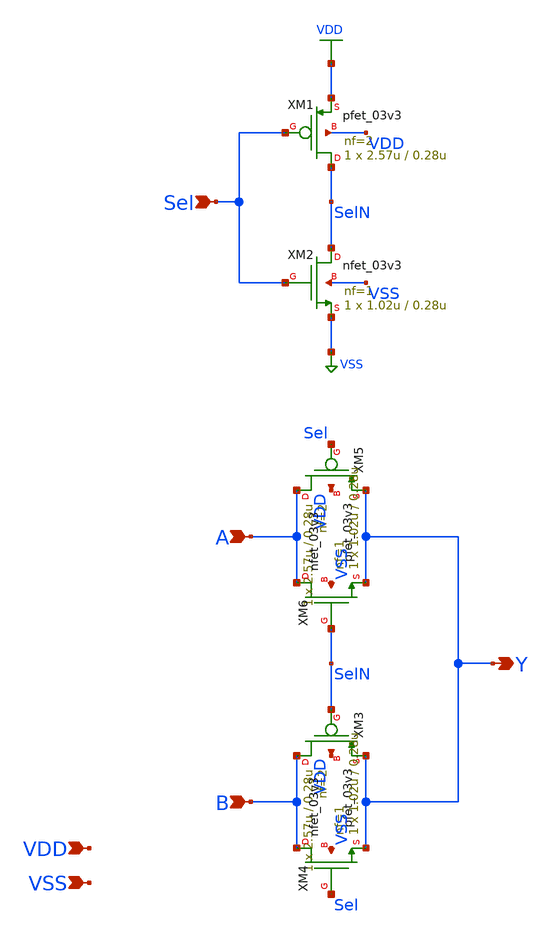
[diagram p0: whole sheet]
** sch_path: xschem/gf180mcu_ocd_sc_rt12t3v3__mux2_1.sch
**.subckt gf180mcu_ocd_sc_rt12t3v3__mux2_1 A B Sel Y VDD VSS
*.ipin A
*.ipin B
*.ipin Sel
*.opin Y
*.ipin VDD
*.ipin VSS
XM1 SelN Sel VDD VDD pfet_03v3 L=0.28u W=2.57u nf=2 ad='int((nf+1)/2) * W/nf * 0.18u' as='int((nf+2)/2) * W/nf * 0.18u'
+ pd='2*int((nf+1)/2) * (W/nf + 0.18u)' ps='2*int((nf+2)/2) * (W/nf + 0.18u)' nrd='0.18u / W' nrs='0.18u / W'
+ sa=0 sb=0 sd=0 m=1
XM2 SelN Sel VSS VSS nfet_03v3 L=0.28u W=1.02u nf=1 ad='int((nf+1)/2) * W/nf * 0.18u' as='int((nf+2)/2) * W/nf * 0.18u'
+ pd='2*int((nf+1)/2) * (W/nf + 0.18u)' ps='2*int((nf+2)/2) * (W/nf + 0.18u)' nrd='0.18u / W' nrs='0.18u / W'
+ sa=0 sb=0 sd=0 m=1
XM3 B SelN Y VDD pfet_03v3 L=0.28u W=2.57u nf=2 ad='int((nf+1)/2) * W/nf * 0.18u' as='int((nf+2)/2) * W/nf * 0.18u'
+ pd='2*int((nf+1)/2) * (W/nf + 0.18u)' ps='2*int((nf+2)/2) * (W/nf + 0.18u)' nrd='0.18u / W' nrs='0.18u / W'
+ sa=0 sb=0 sd=0 m=1
XM4 B Sel Y VSS nfet_03v3 L=0.28u W=1.02u nf=1 ad='int((nf+1)/2) * W/nf * 0.18u' as='int((nf+2)/2) * W/nf * 0.18u'
+ pd='2*int((nf+1)/2) * (W/nf + 0.18u)' ps='2*int((nf+2)/2) * (W/nf + 0.18u)' nrd='0.18u / W' nrs='0.18u / W'
+ sa=0 sb=0 sd=0 m=1
XM5 A Sel Y VDD pfet_03v3 L=0.28u W=2.57u nf=2 ad='int((nf+1)/2) * W/nf * 0.18u' as='int((nf+2)/2) * W/nf * 0.18u'
+ pd='2*int((nf+1)/2) * (W/nf + 0.18u)' ps='2*int((nf+2)/2) * (W/nf + 0.18u)' nrd='0.18u / W' nrs='0.18u / W'
+ sa=0 sb=0 sd=0 m=1
XM6 A SelN Y VSS nfet_03v3 L=0.28u W=1.02u nf=1 ad='int((nf+1)/2) * W/nf * 0.18u' as='int((nf+2)/2) * W/nf * 0.18u'
+ pd='2*int((nf+1)/2) * (W/nf + 0.18u)' ps='2*int((nf+2)/2) * (W/nf + 0.18u)' nrd='0.18u / W' nrs='0.18u / W'
+ sa=0 sb=0 sd=0 m=1
**.ends
.GLOBAL VDD
.GLOBAL VSS
.end
